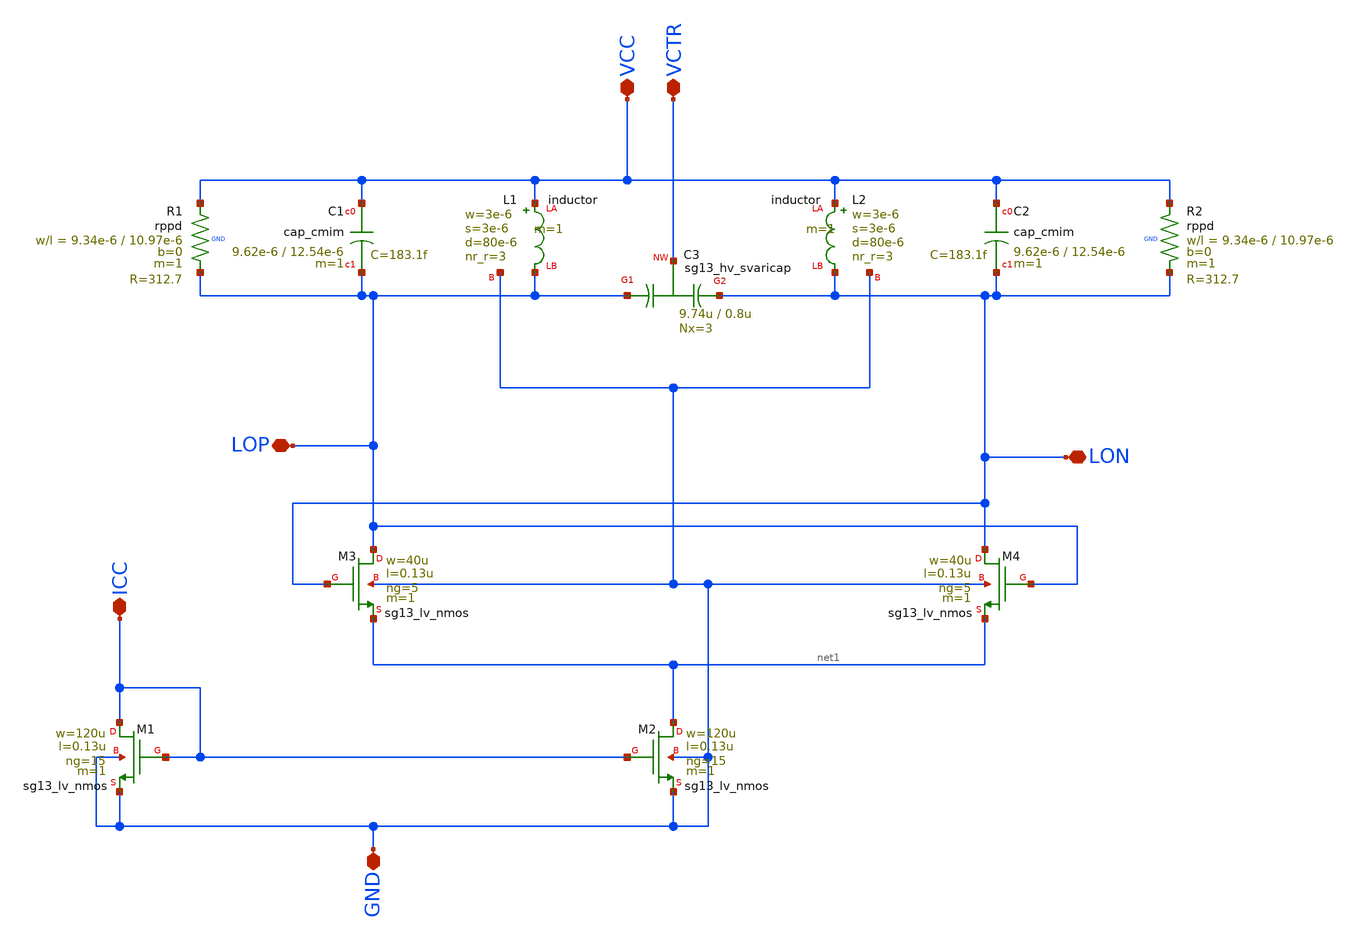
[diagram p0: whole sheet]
** sch_path: OSC0497-main/schematic/xschem/cryovco.sch
**.subckt cryovco VCC LOP GND VCTR ICC LON
*.iopin VCC
*.iopin LOP
*.iopin GND
*.iopin VCTR
*.iopin ICC
*.iopin LON
XL1 VCC LOP GND inductor w=3e-6 s=3e-6 d=80e-6 nr_r=3 m=1
XR1 VCC LOP GND rppd w=9.34e-6 l=10.97e-6 m=1 b=0 mm_ok=1
XC1 VCC LOP cap_cmim w=9.62e-6 l=12.54e-6 m=1 mm_ok=1
XL2 VCC LON GND inductor w=3e-6 s=3e-6 d=80e-6 nr_r=3 m=1
XR2 VCC LON GND rppd w=9.34e-6 l=10.97e-6 m=1 b=0 mm_ok=1
XC2 VCC LON cap_cmim w=9.62e-6 l=12.54e-6 m=1 mm_ok=1
XC3 LOP VCTR LON sub! sg13_hv_svaricap w=9.74u l=0.8u Nx=3 mm_ok=1
XM3 LOP LON net1 GND sg13_lv_nmos w=40u l=0.13u ng=5 m=1 mm_ok=1
XM4 LON LOP net1 GND sg13_lv_nmos w=40u l=0.13u ng=5 m=1 mm_ok=1
XM2 net1 ICC GND GND sg13_lv_nmos w=120u l=0.13u ng=15 m=1 mm_ok=1
XM1 ICC ICC GND GND sg13_lv_nmos w=120u l=0.13u ng=15 m=1 mm_ok=1
**.ends
.end
